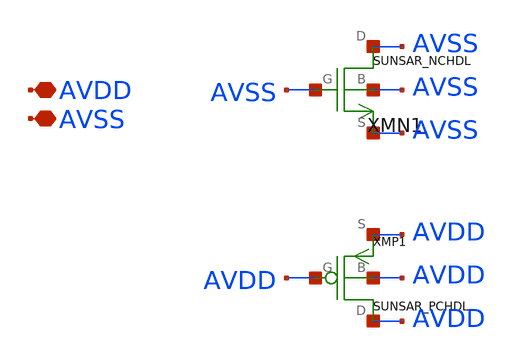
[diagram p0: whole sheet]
** sch_path: ip/sun_sar9b_sky130nm/design/SUN_SAR9B_SKY130NM/SUNSAR_TAPCELLB_CV.sch
**.subckt SUNSAR_TAPCELLB_CV AVDD AVSS
*.iopin AVDD
*.iopin AVSS
XMN1 AVSS AVSS AVSS AVSS SUNSAR_NCHDL
XMP1 AVDD AVDD AVDD AVDD SUNSAR_PCHDL
**.ends
.end
